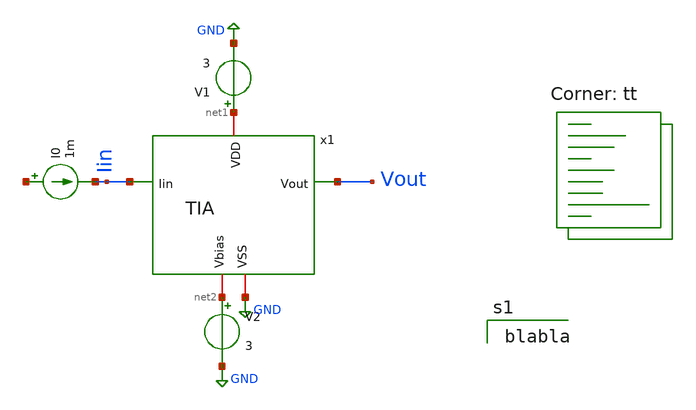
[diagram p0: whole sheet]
** sch_path: analog/library/TIAs/template/TIA_tb.sch
**.subckt TIA_tb
x1 net1 Iin Vout GND net2 TIA
I0 net3 Iin 1m
V1 net1 GND 3
V2 net2 GND 3
**** begin user architecture code

blabla

.lib $::SKYWATER_MODELS/sky130.lib.spice tt
**** end user architecture code
**.ends
.GLOBAL GND
.end
